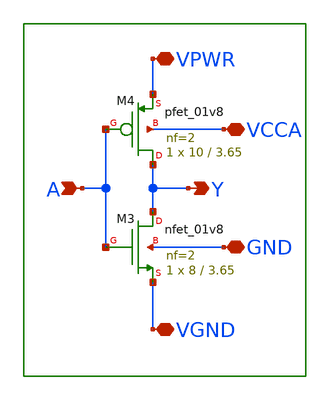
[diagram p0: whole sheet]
** sch_path: xschem/lib/vco_main_inv.sch
**.subckt vco_main_inv VPWR VGND A Y VCCA GND
*.iopin VPWR
*.iopin VGND
*.ipin A
*.opin Y
*.iopin VCCA
*.iopin GND
XM3 Y A VGND GND sky130_fd_pr__nfet_01v8 L=3.65 W=8 nf=2 ad='int((nf+1)/2) * W/nf * 0.29' as='int((nf+2)/2) * W/nf * 0.29'
+ pd='2*int((nf+1)/2) * (W/nf + 0.29)' ps='2*int((nf+2)/2) * (W/nf + 0.29)' nrd='0.29 / W' nrs='0.29 / W'
+ sa=0 sb=0 sd=0 mult=1 m=1
XM4 Y A VPWR VCCA sky130_fd_pr__pfet_01v8 L=3.65 W=10 nf=2 ad='int((nf+1)/2) * W/nf * 0.29' as='int((nf+2)/2) * W/nf * 0.29'
+ pd='2*int((nf+1)/2) * (W/nf + 0.29)' ps='2*int((nf+2)/2) * (W/nf + 0.29)' nrd='0.29 / W' nrs='0.29 / W'
+ sa=0 sb=0 sd=0 mult=1 m=1
**.ends
.end
